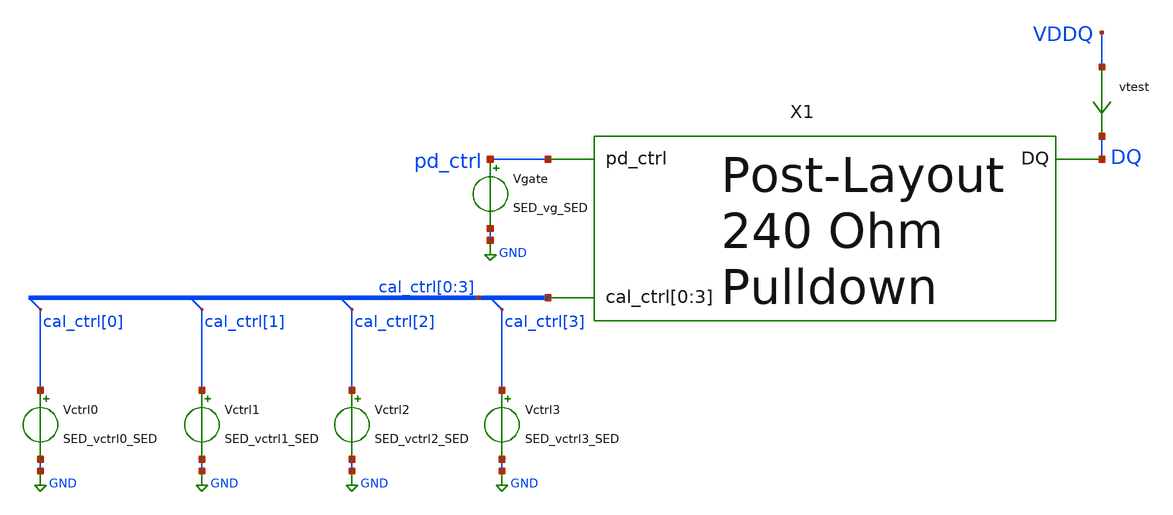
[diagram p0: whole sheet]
** sch_path: schem/post_layout_n-leg_tb.sch
* Copyright 2021 Stefan Frederik Schippers
* Licensed under the Apache License, Version 2.0 (the "License");
* you may not use this file except in compliance with the License.
* You may obtain a copy of the License at
* https://www.apache.org/licenses/LICENSE-2.0
* Unless required by applicable law or agreed to in writing, software
* distributed under the License is distributed on an "AS IS" BASIS,
* WITHOUT WARRANTIES OR CONDITIONS OF ANY KIND, either express or implied.
* See the License for the specific language governing permissions and
* limitations under the License.
**.subckt post_layout_n-leg_tb
vtest VDDQ DQ 0
.save i(vtest)
Vgate pd_ctrl GND SED_vg_SED
Vctrl0 cal_ctrl[0] GND SED_vctrl0_SED
Vctrl1 cal_ctrl[1] GND SED_vctrl1_SED
Vctrl2 cal_ctrl[2] GND SED_vctrl2_SED
Vctrl3 cal_ctrl[3] GND SED_vctrl3_SED
X1 pd_ctrl DQ cal_ctrl[0] cal_ctrl[1] cal_ctrl[2] cal_ctrl[3] GND n-leg_flat
**** begin user architecture code
 ** Local library links to pdk
.lib ./sky130/libs/SED_process_SED_lib.spice SED_process_SED
.include ./layout/pex_n-leg.spice

**** end user architecture code
**.ends
.GLOBAL GND
**** begin user architecture code



* power voltage
vvddq VDDQ 0 0

.control
save all
set temp=SED_temp_SED

* RUN SIMULATION
dc vvddq 0.3 1.2 0.05
* OUTPUT
print v(vddq)/i(vtest)
wrdata out/SED_plotName_SED/SED_plotName_SED.txt v(vddq)/i(vtest)
set hcopydevtype = svg
hardcopy ./out/SED_plotName_SED/SED_plotName_SED.svg vddq/I(vtest) vs vddq title 'Resistance vs pin voltage'

.endc


**** end user architecture code
.end
